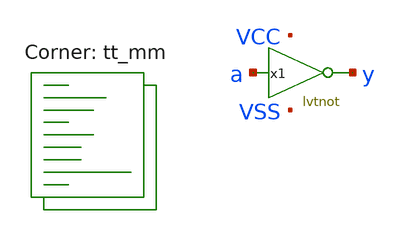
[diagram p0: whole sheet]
** sch_path: xschem/tb_lvtnot.sch
* xschem/lvtnot.sym:
* Copyright 2021 Stefan Frederik Schippers
* Licensed under the Apache License, Version 2.0 (the "License");
**.subckt tb_lvtnot
x1 a y VCC VSS lvtnot W_N=1 L_N=0.15 W_P=2 L_P=0.35 m=1
**** begin user architecture code
.lib $::SKYWATER_MODELS/sky130.lib.spice tt_mm


** this experimental option enables mos model bin
** selection based on W/NF instead of W
.option chgtol=4e-16 method=gear

.param VCCGAUSS = agauss(1.8, 0.05, 1)
.param VCC = 'VCCGAUSS'
** use following line to remove VCC variations
* .param VCC = 1.8
.param VDLGAUSS = agauss(0.9, 0.23, 1)
.param VDL = VDLGAUSS
** use following line to remove input common mode variations
* .param VDL =  0.9
.param TEMPGAUSS = agauss(40, 30, 1)
.option temp = 'TEMPGAUSS'
** use following line to remove temperature variations
* .option temp = 25
.param DELTA = 0.002

.include stimuli_tb_lvtnot.cir

.control
  setseed  8
  reset
  let run = 1
  save all
  op
  write tb_lvtnot.raw
  reset
  set appendwrite
  dowhile run < = 5
    save all
    tran 1n 1000n uic
    write tb_lvtnot.raw
    let run = run + 1
    reset
  end
  quit 0
.endc


**** end user architecture code
**.ends

* expanding   symbol:  /home/ttuser/wowa/xschem/lvtnot.sym # of pins=2
** sym_path: xschem/lvtnot.sym
** sch_path: xschem/lvtnot.sch
.subckt lvtnot a y VCCPIN VSSPIN     W_N=1 L_N=0.15 W_P=2 L_P=0.35
*.opin y
*.ipin a
XM2 y a VCCPIN VCCPIN sky130_fd_pr__pfet_01v8_lvt L=0.35 W=2 nf=1 ad='int((1 + 1)/2) * 2 / 1 * 0.29'
+ as='int((1 + 2)/2) * 2 / 1 * 0.29' pd='2*int((1 + 1)/2) * (2 / 1 + 0.29)' ps='2*int((1 + 2)/2) * (2 / 1 + 0.29)'
+ nrd='0.29 / 2 ' nrs='0.29 / 2 ' sa=0 sb=0 sd=0 mult=1 m=1
XM1 y a VSSPIN VSSPIN sky130_fd_pr__nfet_01v8_lvt L=0.15 W=1 nf=1 ad='int((1 + 1)/2) * 1 / 1 * 0.29'
+ as='int((1 + 2)/2) * 1 / 1 * 0.29' pd='2*int((1 + 1)/2) * (1 / 1 + 0.29)' ps='2*int((1 + 2)/2) * (1 / 1 + 0.29)'
+ nrd='0.29 / 1 ' nrs='0.29 / 1 ' sa=0 sb=0 sd=0 mult=1 m=1
.ends

.end
